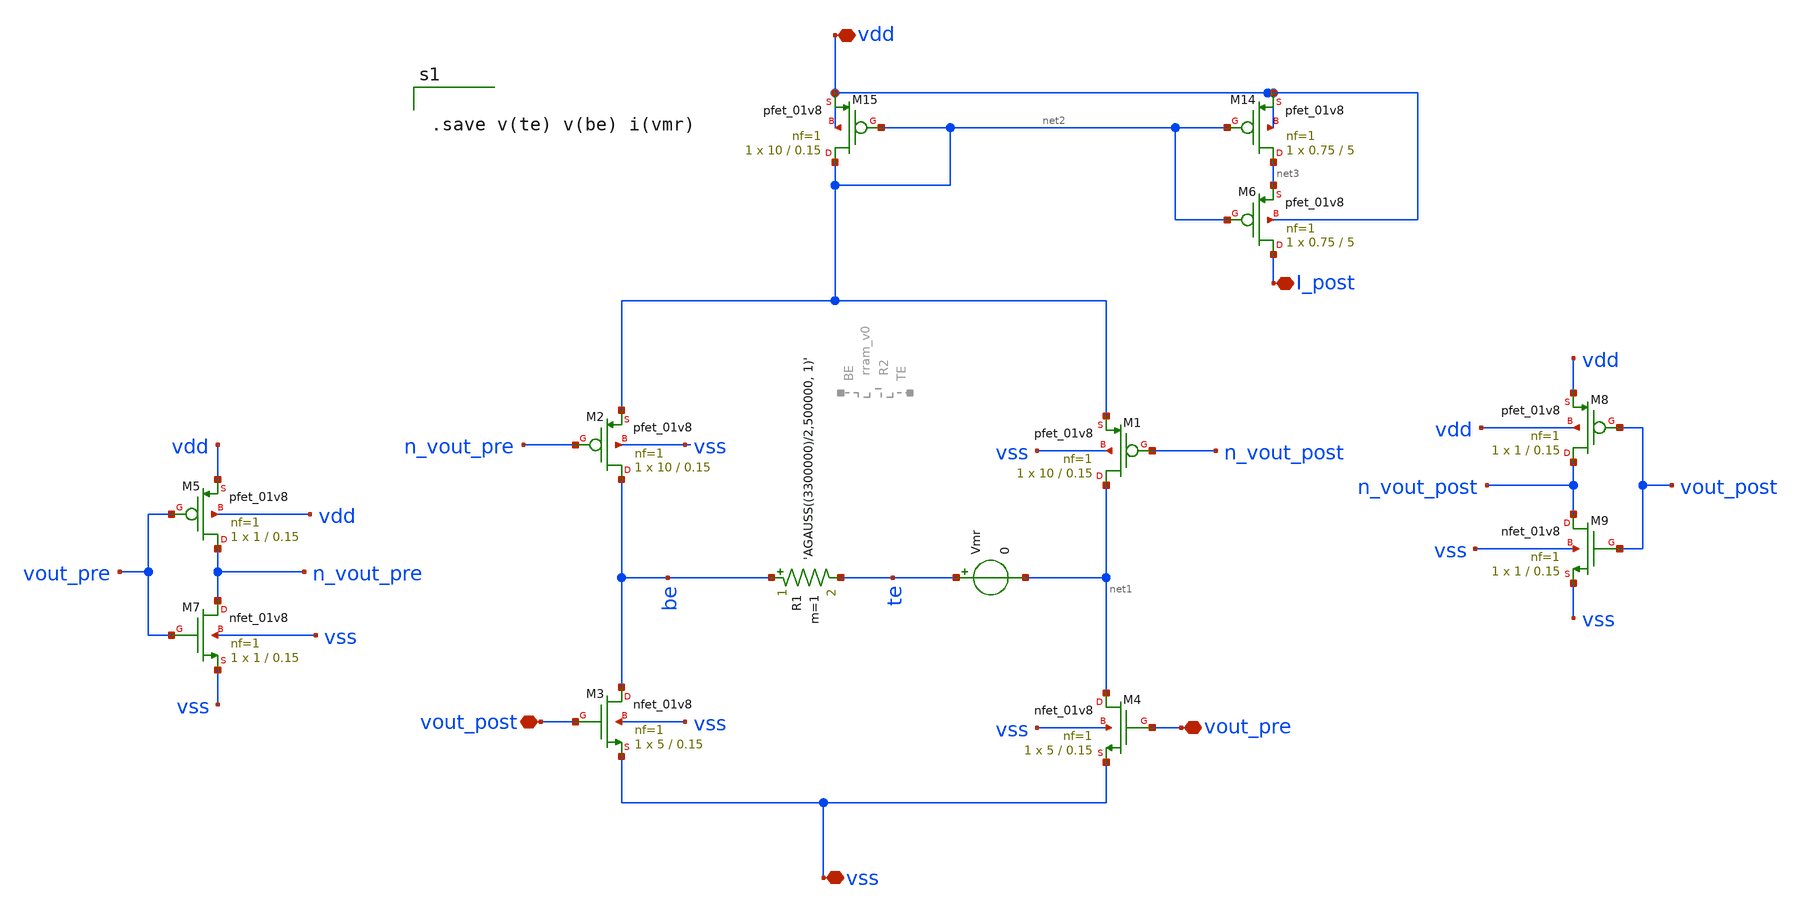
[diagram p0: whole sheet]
** sch_path: Synapse/no_stdp.sch
**.subckt no_stdp vdd vss vout_post vout_pre I_post
*.iopin vdd
*.iopin vss
*.iopin vout_post
*.iopin vout_pre
*.iopin I_post
XM3 be vout_post vss vss sky130_fd_pr__nfet_01v8 L=0.15 W=5 nf=1 ad='int((nf+1)/2) * W/nf * 0.29' as='int((nf+2)/2) * W/nf * 0.29'
+ pd='2*int((nf+1)/2) * (W/nf + 0.29)' ps='2*int((nf+2)/2) * (W/nf + 0.29)' nrd='0.29 / W' nrs='0.29 / W'
+ sa=0 sb=0 sd=0 mult=1 m=1
XM4 net1 vout_pre vss vss sky130_fd_pr__nfet_01v8 L=0.15 W=5 nf=1 ad='int((nf+1)/2) * W/nf * 0.29' as='int((nf+2)/2) * W/nf * 0.29'
+ pd='2*int((nf+1)/2) * (W/nf + 0.29)' ps='2*int((nf+2)/2) * (W/nf + 0.29)' nrd='0.29 / W' nrs='0.29 / W'
+ sa=0 sb=0 sd=0 mult=1 m=1
XM14 net3 net2 vdd vdd sky130_fd_pr__pfet_01v8 L=5 W=0.75 nf=1 ad='int((nf+1)/2) * W/nf * 0.29' as='int((nf+2)/2) * W/nf * 0.29'
+ pd='2*int((nf+1)/2) * (W/nf + 0.29)' ps='2*int((nf+2)/2) * (W/nf + 0.29)' nrd='0.29 / W' nrs='0.29 / W'
+ sa=0 sb=0 sd=0 mult=1 m=1
XM15 net2 net2 vdd vdd sky130_fd_pr__pfet_01v8 L=0.15 W=10 nf=1 ad='int((nf+1)/2) * W/nf * 0.29' as='int((nf+2)/2) * W/nf * 0.29'
+ pd='2*int((nf+1)/2) * (W/nf + 0.29)' ps='2*int((nf+2)/2) * (W/nf + 0.29)' nrd='0.29 / W' nrs='0.29 / W'
+ sa=0 sb=0 sd=0 mult=1 m=1
Vmr te net1 0
.save i(vmr)
XM5 n_vout_pre vout_pre vdd vdd sky130_fd_pr__pfet_01v8 L=0.15 W=1 nf=1 ad='int((nf+1)/2) * W/nf * 0.29'
+ as='int((nf+2)/2) * W/nf * 0.29' pd='2*int((nf+1)/2) * (W/nf + 0.29)' ps='2*int((nf+2)/2) * (W/nf + 0.29)'
+ nrd='0.29 / W' nrs='0.29 / W' sa=0 sb=0 sd=0 mult=1 m=1
XM7 n_vout_pre vout_pre vss vss sky130_fd_pr__nfet_01v8 L=0.15 W=1 nf=1 ad='int((nf+1)/2) * W/nf * 0.29'
+ as='int((nf+2)/2) * W/nf * 0.29' pd='2*int((nf+1)/2) * (W/nf + 0.29)' ps='2*int((nf+2)/2) * (W/nf + 0.29)'
+ nrd='0.29 / W' nrs='0.29 / W' sa=0 sb=0 sd=0 mult=1 m=1
XM8 n_vout_post vout_post vdd vdd sky130_fd_pr__pfet_01v8 L=0.15 W=1 nf=1 ad='int((nf+1)/2) * W/nf * 0.29'
+ as='int((nf+2)/2) * W/nf * 0.29' pd='2*int((nf+1)/2) * (W/nf + 0.29)' ps='2*int((nf+2)/2) * (W/nf + 0.29)'
+ nrd='0.29 / W' nrs='0.29 / W' sa=0 sb=0 sd=0 mult=1 m=1
XM9 n_vout_post vout_post vss vss sky130_fd_pr__nfet_01v8 L=0.15 W=1 nf=1 ad='int((nf+1)/2) * W/nf * 0.29'
+ as='int((nf+2)/2) * W/nf * 0.29' pd='2*int((nf+1)/2) * (W/nf + 0.29)' ps='2*int((nf+2)/2) * (W/nf + 0.29)'
+ nrd='0.29 / W' nrs='0.29 / W' sa=0 sb=0 sd=0 mult=1 m=1
XM1 net1 n_vout_post net2 vss sky130_fd_pr__pfet_01v8 L=0.15 W=10 nf=1 ad='int((nf+1)/2) * W/nf * 0.29'
+ as='int((nf+2)/2) * W/nf * 0.29' pd='2*int((nf+1)/2) * (W/nf + 0.29)' ps='2*int((nf+2)/2) * (W/nf + 0.29)'
+ nrd='0.29 / W' nrs='0.29 / W' sa=0 sb=0 sd=0 mult=1 m=1
XM2 be n_vout_pre net2 vss sky130_fd_pr__pfet_01v8 L=0.15 W=10 nf=1 ad='int((nf+1)/2) * W/nf * 0.29'
+ as='int((nf+2)/2) * W/nf * 0.29' pd='2*int((nf+1)/2) * (W/nf + 0.29)' ps='2*int((nf+2)/2) * (W/nf + 0.29)'
+ nrd='0.29 / W' nrs='0.29 / W' sa=0 sb=0 sd=0 mult=1 m=1
XM6 I_post net2 net3 vdd sky130_fd_pr__pfet_01v8 L=5 W=0.75 nf=1 ad='int((nf+1)/2) * W/nf * 0.29' as='int((nf+2)/2) * W/nf * 0.29'
+ pd='2*int((nf+1)/2) * (W/nf + 0.29)' ps='2*int((nf+2)/2) * (W/nf + 0.29)' nrd='0.29 / W' nrs='0.29 / W'
+ sa=0 sb=0 sd=0 mult=1 m=1
R1 be te 'AGAUSS((3300000)/2,500000, 1)' m=1
**** begin user architecture code


.save v(te) v(be) i(vmr)


**** end user architecture code
**.ends
.end
